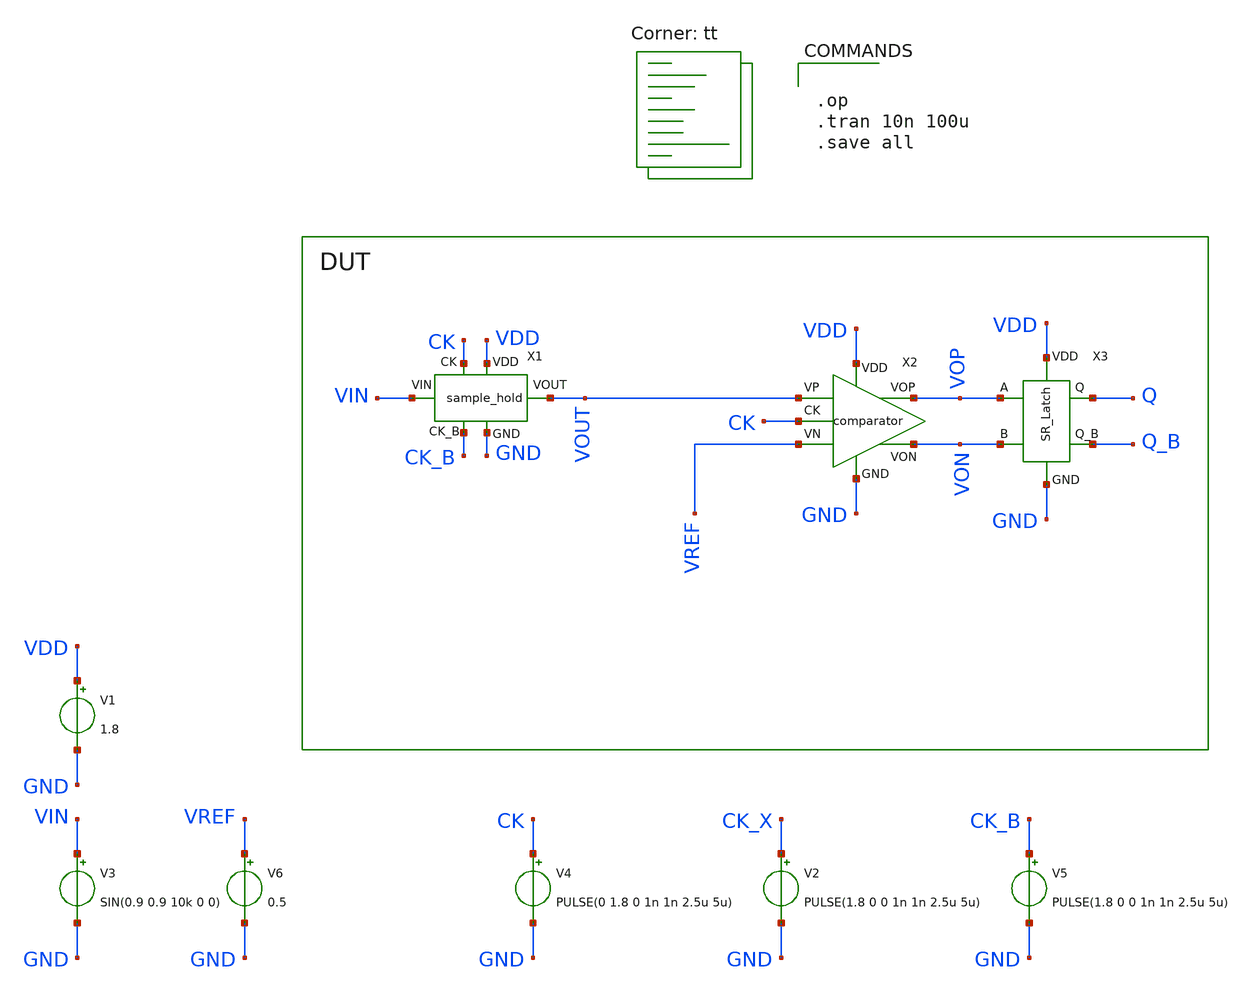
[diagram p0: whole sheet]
** sch_path: xschem/adc_top.sch
**.subckt adc_top
X1 GND VDD VIN VOUT CK CK_B sample_hold
X2 VOUT VREF GND VON VOP VDD CK comparator
X3 VOP VON GND VDD Q Q_B SR_Latch
V1 VDD GND 1.8
V3 VIN GND SIN(0.9 0.9 10k 0 0)
V4 CK GND PULSE(0 1.8 0 1n 1n 2.5u 5u)
V5 CK_B GND PULSE(1.8 0 0 1n 1n 2.5u 5u)
V2 CK_X GND PULSE(1.8 0 0 1n 1n 2.5u 5u)
V6 VREF GND 0.5
**** begin user architecture code
.lib $::SKYWATER_MODELS/sky130.lib.spice tt


.op
.tran 10n 100u
.save all


**** end user architecture code
**.ends
.end
